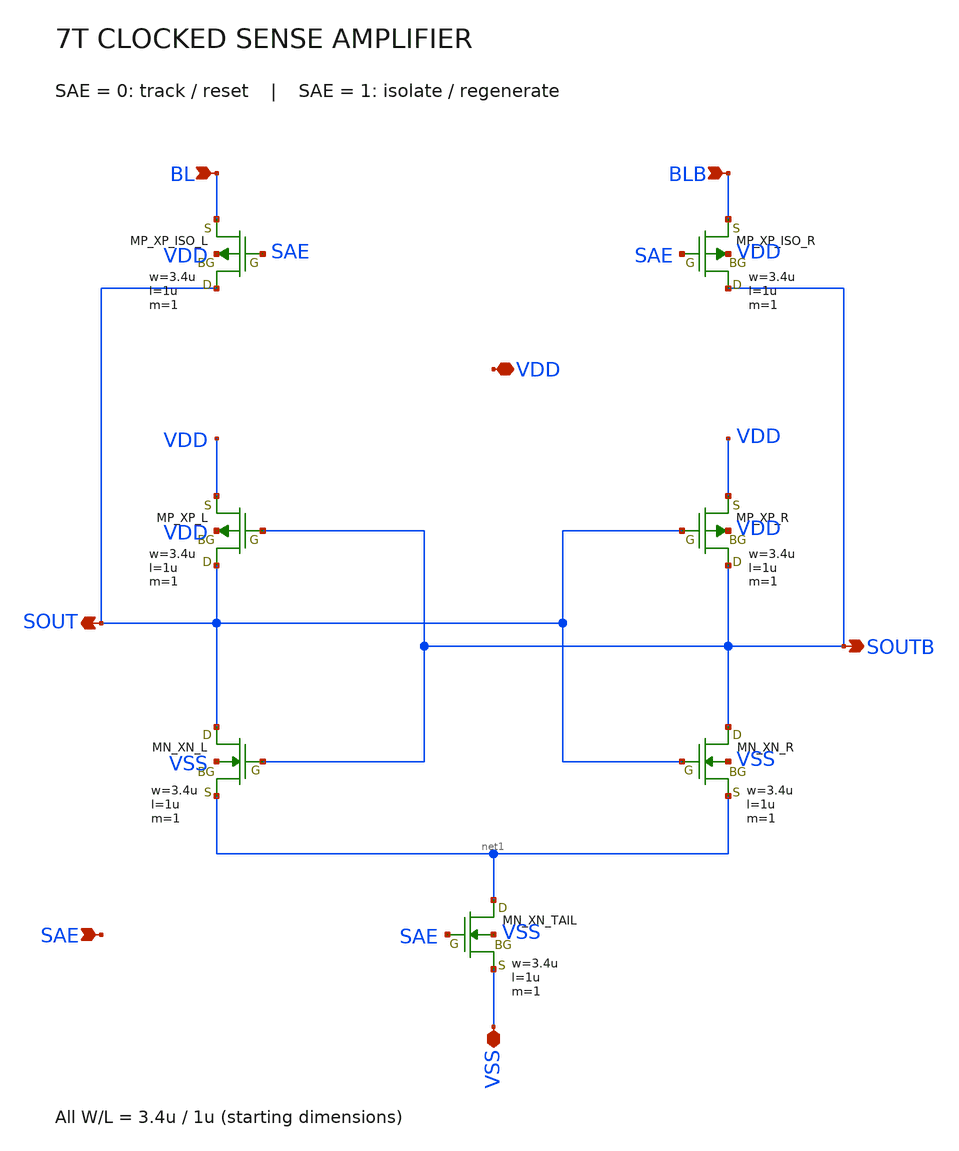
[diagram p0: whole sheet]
** sch_path: member_project/SRAM/PenguinEino/sram512/schematics/sense_amp_7t.sch
**.subckt sense_amp_7t BL BLB SOUT SOUTB VSS VDD SAE
*.ipin BL
*.ipin BLB
*.opin SOUT
*.opin SOUTB
*.iopin VSS
*.iopin VDD
*.ipin SAE
XXP_ISO_L SOUT SAE BL VDD PMOS w=3.4u l=1u nrd=0 nrs=0 m=1
XXP_ISO_R SOUTB SAE BLB VDD PMOS w=3.4u l=1u nrd=0 nrs=0 m=1
XXP_L SOUT SOUTB VDD VDD PMOS w=3.4u l=1u nrd=0 nrs=0 m=1
XXN_L SOUT SOUTB net1 VSS NMOS w=3.4u l=1u nrd=0 nrs=0 m=1
XXP_R SOUTB SOUT VDD VDD PMOS w=3.4u l=1u nrd=0 nrs=0 m=1
XXN_R SOUTB SOUT net1 VSS NMOS w=3.4u l=1u nrd=0 nrs=0 m=1
XXN_TAIL net1 SAE VSS VSS NMOS w=3.4u l=1u nrd=0 nrs=0 m=1
**.ends
.end
